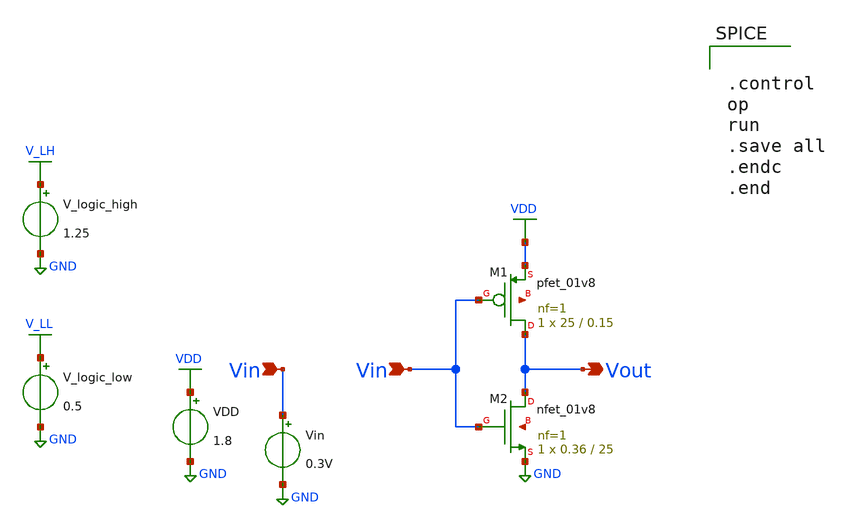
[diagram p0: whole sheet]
** sch_path: xschem/Vth_sch/test_ngspice/test_script1.sch
**.subckt test_script1 Vin Vin Vout
*.ipin Vin
*.ipin Vin
*.opin Vout
VDD VDD GND 1.8
Vin Vin GND 0.3V
XM1 Vout Vin VDD net1 sky130_fd_pr__pfet_01v8 L=0.15 W=25 nf=1 ad='int((nf+1)/2) * W/nf * 0.29' as='int((nf+2)/2) * W/nf * 0.29'
+ pd='2*int((nf+1)/2) * (W/nf + 0.29)' ps='2*int((nf+2)/2) * (W/nf + 0.29)' nrd='0.29 / W' nrs='0.29 / W'
+ sa=0 sb=0 sd=0 mult=1 m=1
XM2 Vout Vin GND net2 sky130_fd_pr__nfet_01v8 L=25 W=0.36 nf=1 ad='int((nf+1)/2) * W/nf * 0.29' as='int((nf+2)/2) * W/nf * 0.29'
+ pd='2*int((nf+1)/2) * (W/nf + 0.29)' ps='2*int((nf+2)/2) * (W/nf + 0.29)' nrd='0.29 / W' nrs='0.29 / W'
+ sa=0 sb=0 sd=0 mult=1 m=1
V_logic_high V_LH GND 1.25
V_logic_low V_LL GND 0.5
**** begin user architecture code


.lib /usr/local/share/pdk/sky130A/libs.tech/ngspice/sky130.lib.spice tt

.save all





.control
op
run
.save all
.endc
.end


**** end user architecture code
**.ends
.GLOBAL VDD
.GLOBAL GND
.GLOBAL V_LH
.GLOBAL V_LL
.end
